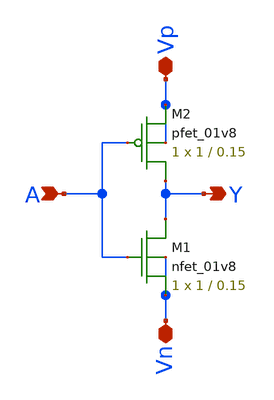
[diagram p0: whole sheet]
** sch_path: xschem/inverter.sch
**.subckt inverter A Vp Vn Y
*.ipin A
*.iopin Vp
*.iopin Vn
*.opin Y
XM1 Y A Vn Vn sky130_fd_pr__nfet_01v8 L=0.15 W=1 nf=1 ad='int((nf+1)/2) * W/nf * 0.29' as='int((nf+2)/2) * W/nf * 0.29'
+ pd='2*int((nf+1)/2) * (W/nf + 0.29)' ps='2*int((nf+2)/2) * (W/nf + 0.29)' nrd='0.29 / W' nrs='0.29 / W'
+ sa=0 sb=0 sd=0 mult=1 m=1
XM2 Y A Vp Vp sky130_fd_pr__pfet_01v8 L=0.15 W=1 nf=1 ad='int((nf+1)/2) * W/nf * 0.29' as='int((nf+2)/2) * W/nf * 0.29'
+ pd='2*int((nf+1)/2) * (W/nf + 0.29)' ps='2*int((nf+2)/2) * (W/nf + 0.29)' nrd='0.29 / W' nrs='0.29 / W'
+ sa=0 sb=0 sd=0 mult=1 m=1
**.ends
.end
